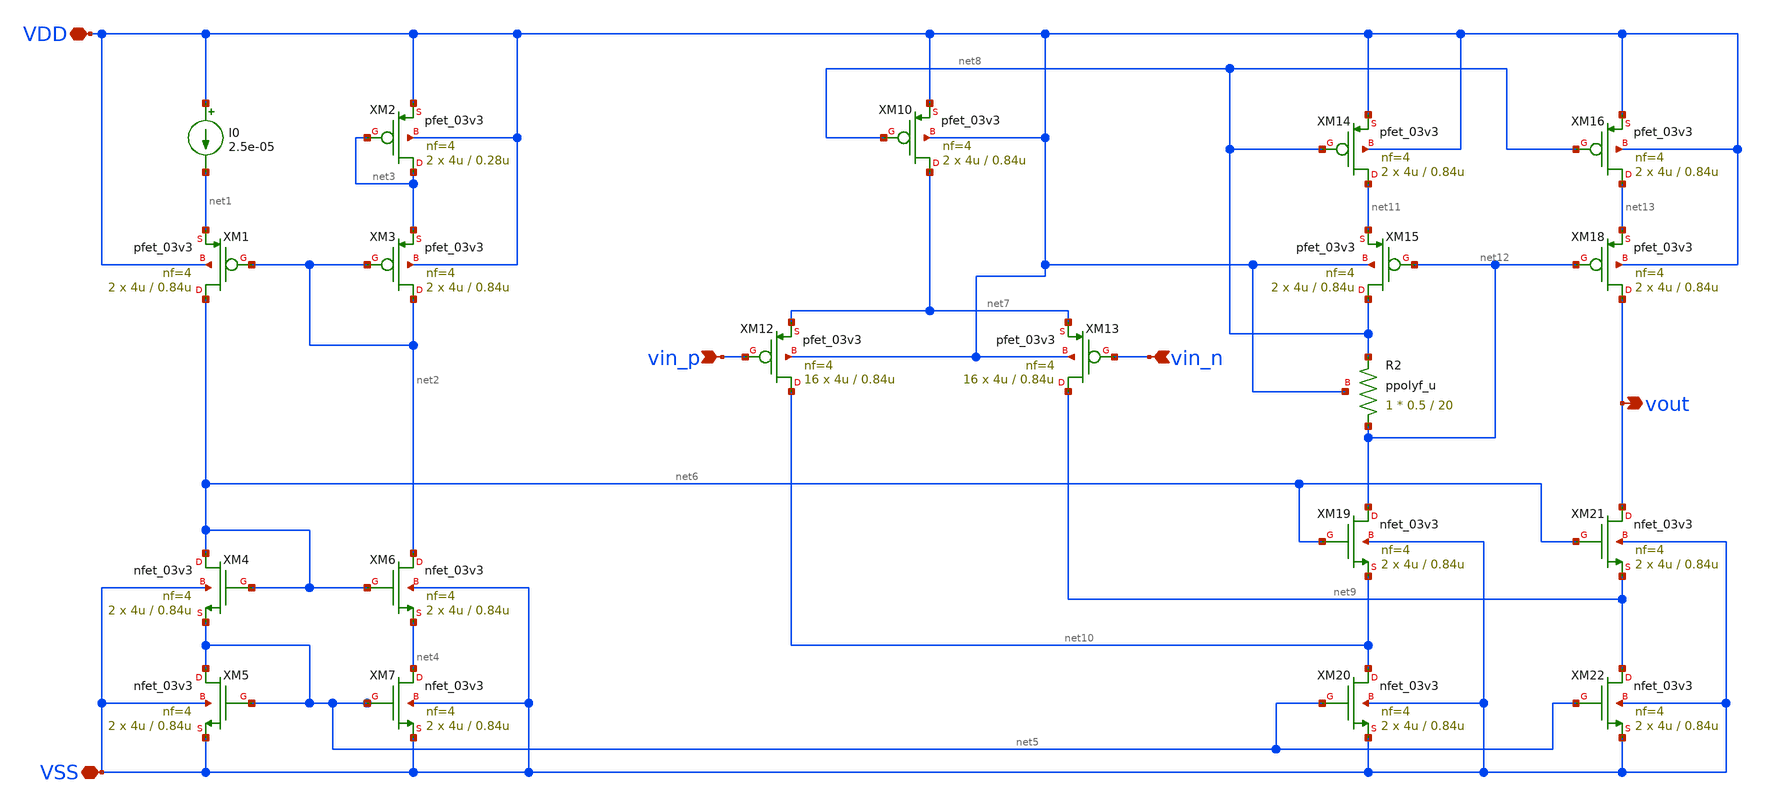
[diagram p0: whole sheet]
** sch_path: xschem/gfmcu_example_amp.sch
**.subckt gfmcu_example_amp vin_n vin_p vout VSS VDD
*.ipin vin_n
*.ipin vin_p
*.opin vout
*.iopin VSS
*.iopin VDD
XM1 net6 net2 net1 VDD pfet_03v3 L=0.84u W=4u nf=4 ad='int((nf+1)/2) * W/nf * 0.18u' as='int((nf+2)/2) * W/nf * 0.18u'
+ pd='2*int((nf+1)/2) * (W/nf + 0.18u)' ps='2*int((nf+2)/2) * (W/nf + 0.18u)' nrd='0.18u / W' nrs='0.18u / W'
+ sa=0 sb=0 sd=0 m=2 par=2
XM2 net3 net3 VDD VDD pfet_03v3 L=0.28u W=4u nf=4 ad='int((nf+1)/2) * W/nf * 0.18u' as='int((nf+2)/2) * W/nf * 0.18u'
+ pd='2*int((nf+1)/2) * (W/nf + 0.18u)' ps='2*int((nf+2)/2) * (W/nf + 0.18u)' nrd='0.18u / W' nrs='0.18u / W'
+ sa=0 sb=0 sd=0 m=2 par=2
XM3 net2 net2 net3 VDD pfet_03v3 L=0.84u W=4u nf=4 ad='int((nf+1)/2) * W/nf * 0.18u' as='int((nf+2)/2) * W/nf * 0.18u'
+ pd='2*int((nf+1)/2) * (W/nf + 0.18u)' ps='2*int((nf+2)/2) * (W/nf + 0.18u)' nrd='0.18u / W' nrs='0.18u / W'
+ sa=0 sb=0 sd=0 m=2 par=2
XM4 net6 net6 net5 VSS nfet_03v3 L=0.84u W=4u nf=4 ad='int((nf+1)/2) * W/nf * 0.18u' as='int((nf+2)/2) * W/nf * 0.18u'
+ pd='2*int((nf+1)/2) * (W/nf + 0.18u)' ps='2*int((nf+2)/2) * (W/nf + 0.18u)' nrd='0.18u / W' nrs='0.18u / W'
+ sa=0 sb=0 sd=0 m=2 par=2
XM5 net5 net5 VSS VSS nfet_03v3 L=0.84u W=4u nf=4 ad='int((nf+1)/2) * W/nf * 0.18u' as='int((nf+2)/2) * W/nf * 0.18u'
+ pd='2*int((nf+1)/2) * (W/nf + 0.18u)' ps='2*int((nf+2)/2) * (W/nf + 0.18u)' nrd='0.18u / W' nrs='0.18u / W'
+ sa=0 sb=0 sd=0 m=2 par=2
XM6 net2 net6 net4 VSS nfet_03v3 L=0.84u W=4u nf=4 ad='int((nf+1)/2) * W/nf * 0.18u' as='int((nf+2)/2) * W/nf * 0.18u'
+ pd='2*int((nf+1)/2) * (W/nf + 0.18u)' ps='2*int((nf+2)/2) * (W/nf + 0.18u)' nrd='0.18u / W' nrs='0.18u / W'
+ sa=0 sb=0 sd=0 m=2 par=2
XM7 net4 net5 VSS VSS nfet_03v3 L=0.84u W=4u nf=4 ad='int((nf+1)/2) * W/nf * 0.18u' as='int((nf+2)/2) * W/nf * 0.18u'
+ pd='2*int((nf+1)/2) * (W/nf + 0.18u)' ps='2*int((nf+2)/2) * (W/nf + 0.18u)' nrd='0.18u / W' nrs='0.18u / W'
+ sa=0 sb=0 sd=0 m=2 par=2
XM10 net7 net8 VDD VDD pfet_03v3 L=0.84u W=4u nf=4 ad='int((nf+1)/2) * W/nf * 0.18u' as='int((nf+2)/2) * W/nf * 0.18u'
+ pd='2*int((nf+1)/2) * (W/nf + 0.18u)' ps='2*int((nf+2)/2) * (W/nf + 0.18u)' nrd='0.18u / W' nrs='0.18u / W'
+ sa=0 sb=0 sd=0 m=2 par=2
XM12 net10 vin_p net7 VDD pfet_03v3 L=0.84u W=4u nf=4 ad='int((nf+1)/2) * W/nf * 0.18u' as='int((nf+2)/2) * W/nf * 0.18u'
+ pd='2*int((nf+1)/2) * (W/nf + 0.18u)' ps='2*int((nf+2)/2) * (W/nf + 0.18u)' nrd='0.18u / W' nrs='0.18u / W'
+ sa=0 sb=0 sd=0 m=16 par=16
XM13 net9 vin_n net7 VDD pfet_03v3 L=0.84u W=4u nf=4 ad='int((nf+1)/2) * W/nf * 0.18u' as='int((nf+2)/2) * W/nf * 0.18u'
+ pd='2*int((nf+1)/2) * (W/nf + 0.18u)' ps='2*int((nf+2)/2) * (W/nf + 0.18u)' nrd='0.18u / W' nrs='0.18u / W'
+ sa=0 sb=0 sd=0 m=16 par=16
XM14 net11 net8 VDD VDD pfet_03v3 L=0.84u W=4u nf=4 ad='int((nf+1)/2) * W/nf * 0.18u' as='int((nf+2)/2) * W/nf * 0.18u'
+ pd='2*int((nf+1)/2) * (W/nf + 0.18u)' ps='2*int((nf+2)/2) * (W/nf + 0.18u)' nrd='0.18u / W' nrs='0.18u / W'
+ sa=0 sb=0 sd=0 m=2 par=2
XM15 net8 net12 net11 VDD pfet_03v3 L=0.84u W=4u nf=4 ad='int((nf+1)/2) * W/nf * 0.18u' as='int((nf+2)/2) * W/nf * 0.18u'
+ pd='2*int((nf+1)/2) * (W/nf + 0.18u)' ps='2*int((nf+2)/2) * (W/nf + 0.18u)' nrd='0.18u / W' nrs='0.18u / W'
+ sa=0 sb=0 sd=0 m=2 par=2
XR2 net12 net8 VDD ppolyf_u r_width=0.5 r_length=20 m=1
XM16 net13 net8 VDD VDD pfet_03v3 L=0.84u W=4u nf=4 ad='int((nf+1)/2) * W/nf * 0.18u' as='int((nf+2)/2) * W/nf * 0.18u'
+ pd='2*int((nf+1)/2) * (W/nf + 0.18u)' ps='2*int((nf+2)/2) * (W/nf + 0.18u)' nrd='0.18u / W' nrs='0.18u / W'
+ sa=0 sb=0 sd=0 m=2 par=2
XM18 vout net12 net13 VDD pfet_03v3 L=0.84u W=4u nf=4 ad='int((nf+1)/2) * W/nf * 0.18u' as='int((nf+2)/2) * W/nf * 0.18u'
+ pd='2*int((nf+1)/2) * (W/nf + 0.18u)' ps='2*int((nf+2)/2) * (W/nf + 0.18u)' nrd='0.18u / W' nrs='0.18u / W'
+ sa=0 sb=0 sd=0 m=2 par=2
XM19 net12 net6 net10 VSS nfet_03v3 L=0.84u W=4u nf=4 ad='int((nf+1)/2) * W/nf * 0.18u' as='int((nf+2)/2) * W/nf * 0.18u'
+ pd='2*int((nf+1)/2) * (W/nf + 0.18u)' ps='2*int((nf+2)/2) * (W/nf + 0.18u)' nrd='0.18u / W' nrs='0.18u / W'
+ sa=0 sb=0 sd=0 m=2 par=2
XM20 net10 net5 VSS VSS nfet_03v3 L=0.84u W=4u nf=4 ad='int((nf+1)/2) * W/nf * 0.18u' as='int((nf+2)/2) * W/nf * 0.18u'
+ pd='2*int((nf+1)/2) * (W/nf + 0.18u)' ps='2*int((nf+2)/2) * (W/nf + 0.18u)' nrd='0.18u / W' nrs='0.18u / W'
+ sa=0 sb=0 sd=0 m=2 par=2
XM21 vout net6 net9 VSS nfet_03v3 L=0.84u W=4u nf=4 ad='int((nf+1)/2) * W/nf * 0.18u' as='int((nf+2)/2) * W/nf * 0.18u'
+ pd='2*int((nf+1)/2) * (W/nf + 0.18u)' ps='2*int((nf+2)/2) * (W/nf + 0.18u)' nrd='0.18u / W' nrs='0.18u / W'
+ sa=0 sb=0 sd=0 m=2 par=2
XM22 net9 net5 VSS VSS nfet_03v3 L=0.84u W=4u nf=4 ad='int((nf+1)/2) * W/nf * 0.18u' as='int((nf+2)/2) * W/nf * 0.18u'
+ pd='2*int((nf+1)/2) * (W/nf + 0.18u)' ps='2*int((nf+2)/2) * (W/nf + 0.18u)' nrd='0.18u / W' nrs='0.18u / W'
+ sa=0 sb=0 sd=0 m=2 par=2
I0 VDD net1 2.5e-05
**.ends
.end
